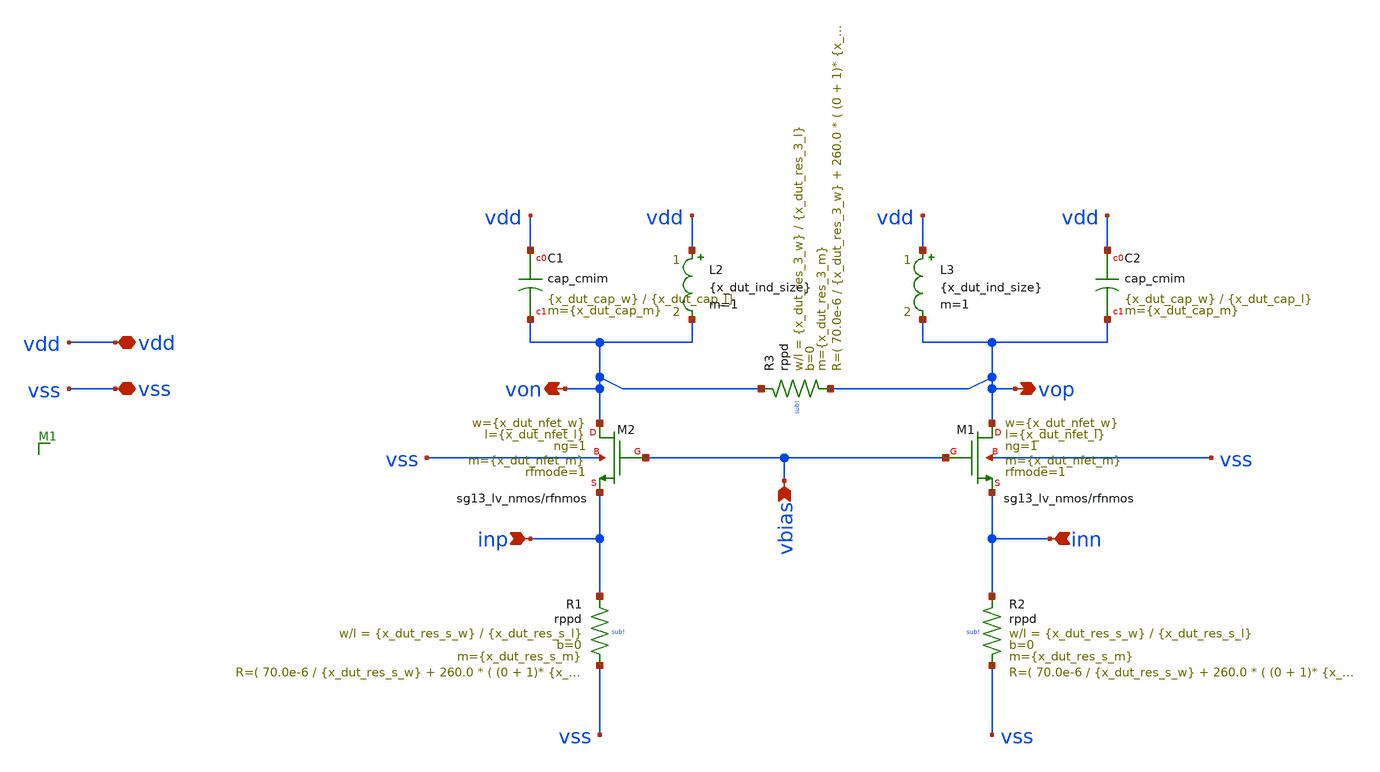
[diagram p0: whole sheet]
** sch_path: examples/tunable-tia/ihp-sg13g2/xschem/tia-topo-1/tia-bpf-1-ideal-ind.sch
**.subckt tia-bpf-1-ideal-ind vdd vss inp inn von vop vbias
*.iopin vdd
*.iopin vss
*.ipin inp
*.ipin inn
*.opin von
*.opin vop
*.ipin vbias
XM1 vop vbias inn vss sg13_lv_nmos w={x_dut_nfet_w} l={x_dut_nfet_l} ng=1 m={x_dut_nfet_m} rfmode=1 mm_ok=1
XM2 von vbias inp vss sg13_lv_nmos w={x_dut_nfet_w} l={x_dut_nfet_l} ng=1 m={x_dut_nfet_m} rfmode=1 mm_ok=1
XC1 vdd von cap_cmim w={x_dut_cap_w} l={x_dut_cap_l} m={x_dut_cap_m} mm_ok=1
XC2 vdd vop cap_cmim w={x_dut_cap_w} l={x_dut_cap_l} m={x_dut_cap_m} mm_ok=1
XR1 inp vss sub! rppd w={x_dut_res_s_w} l={x_dut_res_s_l} m={x_dut_res_s_m} b=0 mm_ok=1
XR2 inn vss sub! rppd w={x_dut_res_s_w} l={x_dut_res_s_l} m={x_dut_res_s_m} b=0 mm_ok=1
XR3 von vop sub! rppd w={x_dut_res_3_w} l={x_dut_res_3_l} m={x_dut_res_3_m} b=0 mm_ok=1
L2 vdd von {x_dut_ind_size} m=1
L3 vdd vop {x_dut_ind_size} m=1
**.ends
.end
